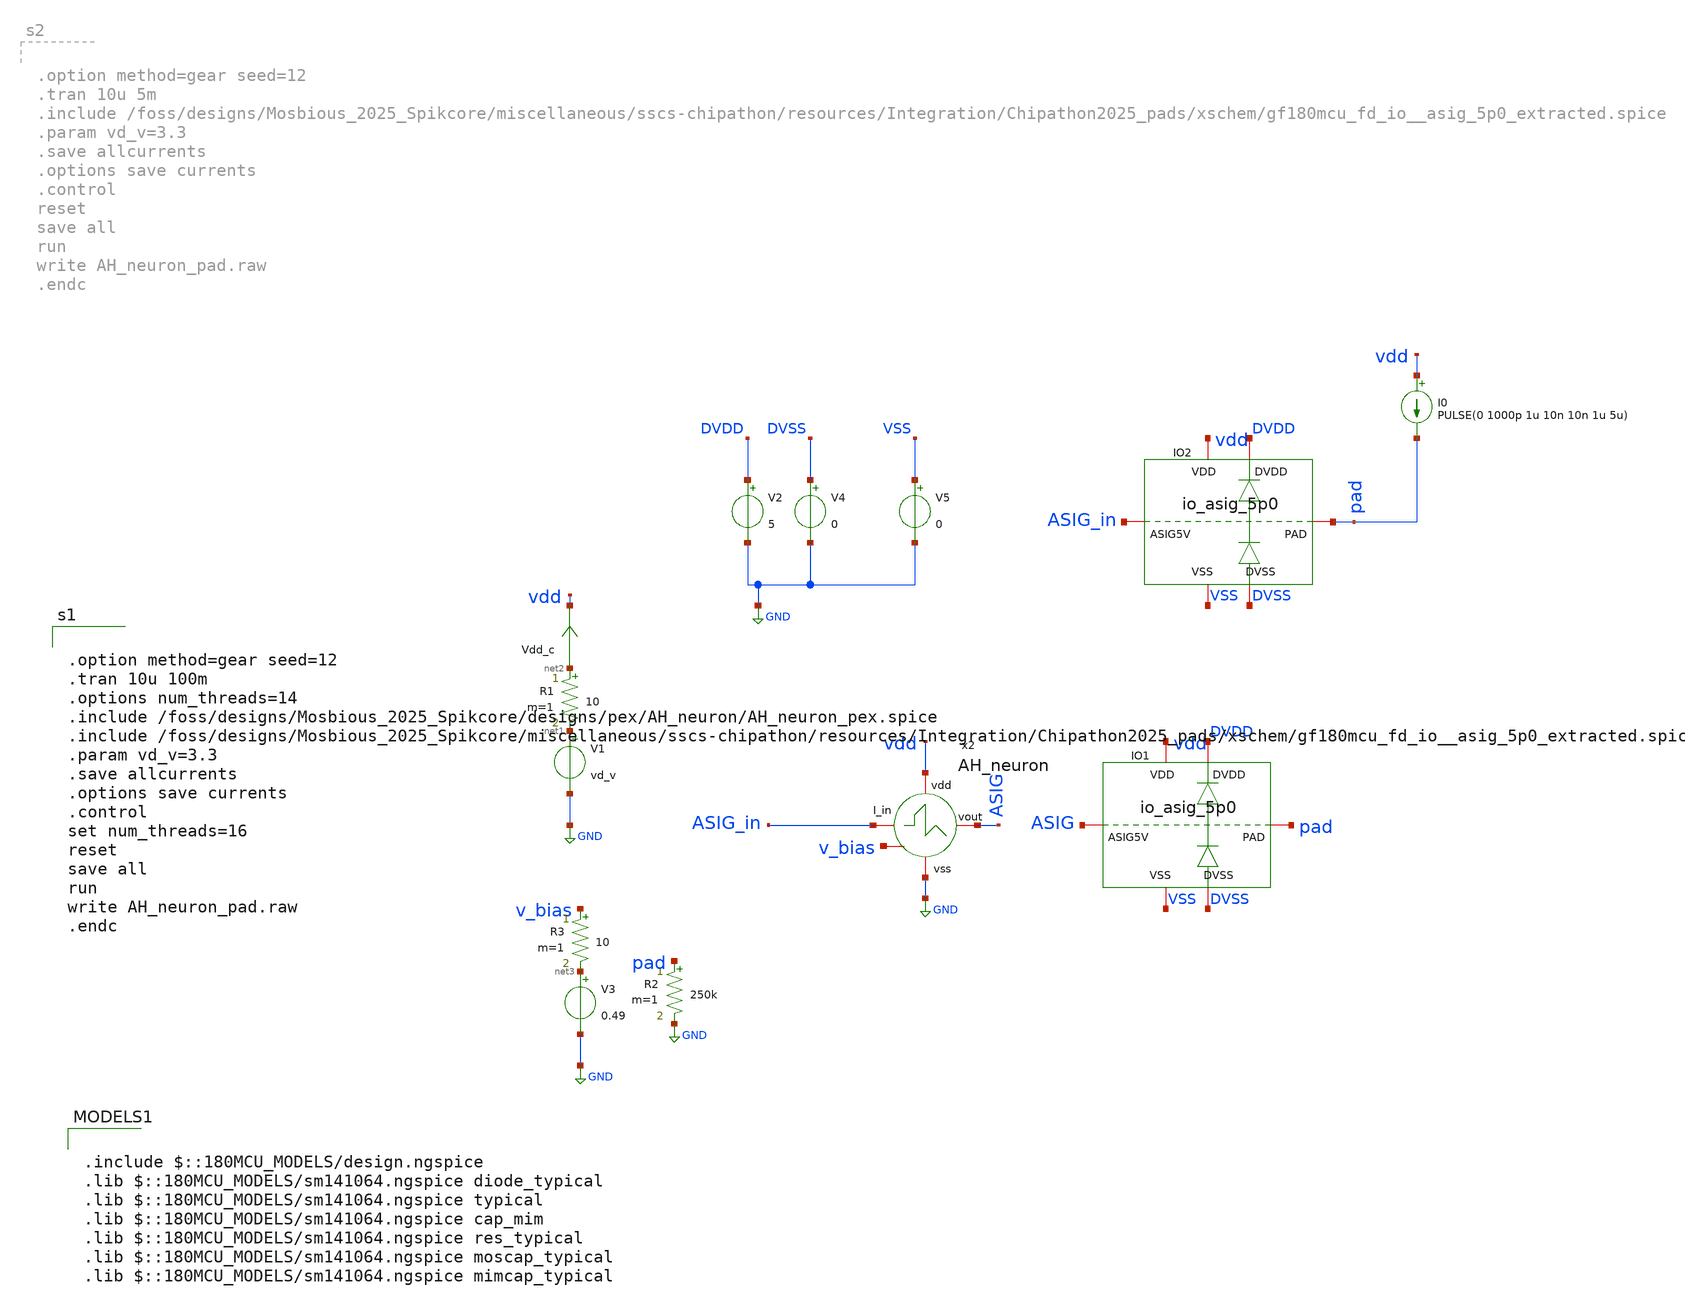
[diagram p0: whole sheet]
** sch_path: designs/libs/tb_core_analogs_pads/tb_AH_neuron/AH_neuron.sch
**.subckt AH_neuron
V1 net1 GND vd_v
Vdd_c net2 vdd 0
.save i(vdd_c)
I0 vdd pad PULSE(0 1000p 1u 10n 10n 1u 5u)
R1 net2 net1 10 m=1
R2 pad GND 250k m=1
V2 DVDD GND 5
V4 DVSS GND 0
V5 VSS GND 0
XIO1 DVSS DVDD VSS vdd pad ASIG gf180mcu_fd_io__asig_5p0_extracted
V3 net3 GND 0.49
R3 v_bias net3 10 m=1
x2 vdd ASIG_in ASIG GND v_bias AH_neuron
XIO2 DVSS DVDD VSS vdd pad ASIG_in gf180mcu_fd_io__asig_5p0_extracted
**** begin user architecture code


.option method=gear seed=12
.tran 10u 100m
.options num_threads=14
.include /foss/designs/Mosbious_2025_Spikcore/designs/pex/AH_neuron/AH_neuron_pex.spice
.include /foss/designs/Mosbious_2025_Spikcore/miscellaneous/sscs-chipathon/resources/Integration/Chipathon2025_pads/xschem/gf180mcu_fd_io__asig_5p0_extracted.spice
.param vd_v=3.3
.save allcurrents
.options save currents
.control
set num_threads=16
reset
save all
run
write AH_neuron_pad.raw
.endc



.include $::180MCU_MODELS/design.ngspice
.lib $::180MCU_MODELS/sm141064.ngspice diode_typical
.lib $::180MCU_MODELS/sm141064.ngspice typical
.lib $::180MCU_MODELS/sm141064.ngspice cap_mim
.lib $::180MCU_MODELS/sm141064.ngspice res_typical
.lib $::180MCU_MODELS/sm141064.ngspice moscap_typical
.lib $::180MCU_MODELS/sm141064.ngspice mimcap_typical

**** end user architecture code
**.ends
.GLOBAL GND
.end
